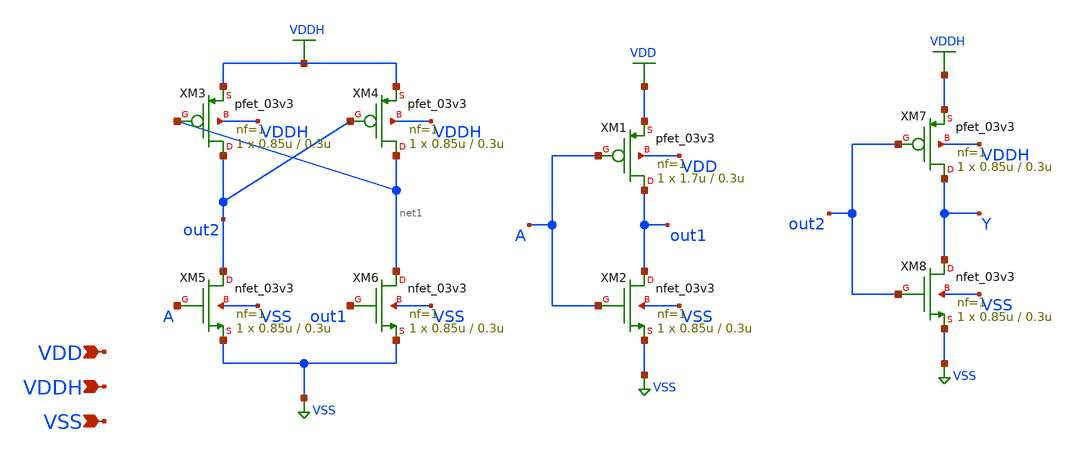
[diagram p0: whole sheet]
** sch_path: gf180mcu_osu_sc_gp12t3v3/xschem/gf180mcu_osu_sc_gp12t3v3__lshifup.sch
**.subckt gf180mcu_osu_sc_gp12t3v3__lshifup VDDH VSS VDD
*.ipin VDDH
*.ipin VSS
*.ipin VDD
XM1 out1 A VDD VDD pfet_03v3 L=0.3u W=1.7u nf=1 ad='int((nf+1)/2) * W/nf * 0.18u' as='int((nf+2)/2) * W/nf * 0.18u'
+ pd='2*int((nf+1)/2) * (W/nf + 0.18u)' ps='2*int((nf+2)/2) * (W/nf + 0.18u)' nrd='0.18u / W' nrs='0.18u / W'
+ sa=0 sb=0 sd=0 m=1
XM2 out1 A VSS VSS nfet_03v3 L=0.3u W=0.85u nf=1 ad='int((nf+1)/2) * W/nf * 0.18u' as='int((nf+2)/2) * W/nf * 0.18u'
+ pd='2*int((nf+1)/2) * (W/nf + 0.18u)' ps='2*int((nf+2)/2) * (W/nf + 0.18u)' nrd='0.18u / W' nrs='0.18u / W'
+ sa=0 sb=0 sd=0 m=1
XM3 out2 net1 VDDH VDDH pfet_03v3 L=0.3u W=0.85u nf=1 ad='int((nf+1)/2) * W/nf * 0.18u' as='int((nf+2)/2) * W/nf * 0.18u'
+ pd='2*int((nf+1)/2) * (W/nf + 0.18u)' ps='2*int((nf+2)/2) * (W/nf + 0.18u)' nrd='0.18u / W' nrs='0.18u / W'
+ sa=0 sb=0 sd=0 m=1
XM4 net1 out2 VDDH VDDH pfet_03v3 L=0.3u W=0.85u nf=1 ad='int((nf+1)/2) * W/nf * 0.18u' as='int((nf+2)/2) * W/nf * 0.18u'
+ pd='2*int((nf+1)/2) * (W/nf + 0.18u)' ps='2*int((nf+2)/2) * (W/nf + 0.18u)' nrd='0.18u / W' nrs='0.18u / W'
+ sa=0 sb=0 sd=0 m=1
XM5 out2 A VSS VSS nfet_03v3 L=0.3u W=0.85u nf=1 ad='int((nf+1)/2) * W/nf * 0.18u' as='int((nf+2)/2) * W/nf * 0.18u'
+ pd='2*int((nf+1)/2) * (W/nf + 0.18u)' ps='2*int((nf+2)/2) * (W/nf + 0.18u)' nrd='0.18u / W' nrs='0.18u / W'
+ sa=0 sb=0 sd=0 m=1
XM6 net1 out1 VSS VSS nfet_03v3 L=0.3u W=0.85u nf=1 ad='int((nf+1)/2) * W/nf * 0.18u' as='int((nf+2)/2) * W/nf * 0.18u'
+ pd='2*int((nf+1)/2) * (W/nf + 0.18u)' ps='2*int((nf+2)/2) * (W/nf + 0.18u)' nrd='0.18u / W' nrs='0.18u / W'
+ sa=0 sb=0 sd=0 m=1
XM7 Y out2 VDDH VDDH pfet_03v3 L=0.3u W=0.85u nf=1 ad='int((nf+1)/2) * W/nf * 0.18u' as='int((nf+2)/2) * W/nf * 0.18u'
+ pd='2*int((nf+1)/2) * (W/nf + 0.18u)' ps='2*int((nf+2)/2) * (W/nf + 0.18u)' nrd='0.18u / W' nrs='0.18u / W'
+ sa=0 sb=0 sd=0 m=1
XM8 Y out2 VSS VSS nfet_03v3 L=0.3u W=0.85u nf=1 ad='int((nf+1)/2) * W/nf * 0.18u' as='int((nf+2)/2) * W/nf * 0.18u'
+ pd='2*int((nf+1)/2) * (W/nf + 0.18u)' ps='2*int((nf+2)/2) * (W/nf + 0.18u)' nrd='0.18u / W' nrs='0.18u / W'
+ sa=0 sb=0 sd=0 m=1
**.ends
.GLOBAL VDD
.GLOBAL VSS
.GLOBAL VDDH
.end
